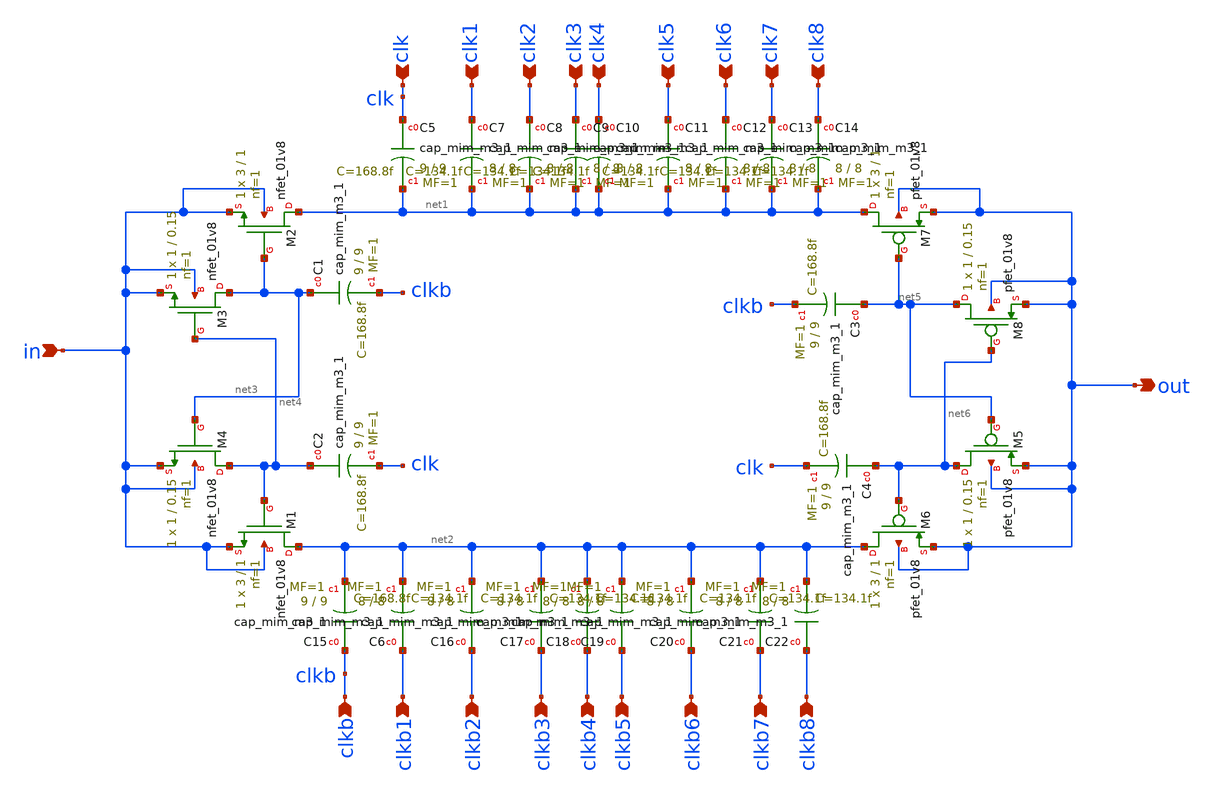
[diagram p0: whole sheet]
** sch_path: xschem/charge_pumps2/CP1.sch
**.subckt CP1 in clk clk1 clk2 clk3 clk4 clk5 clk6 clk7 clk8 clkb clkb1 clkb2 clkb3 clkb4 clkb5
*+ clkb6 clkb7 clkb8 out
*.ipin in
*.ipin clk
*.ipin clk1
*.ipin clk2
*.ipin clk3
*.ipin clk4
*.ipin clk5
*.ipin clk6
*.ipin clk7
*.ipin clk8
*.ipin clkb
*.ipin clkb1
*.ipin clkb2
*.ipin clkb3
*.ipin clkb4
*.ipin clkb5
*.ipin clkb6
*.ipin clkb7
*.ipin clkb8
*.opin out
XM2 net1 net3 in in sky130_fd_pr__nfet_01v8 L=1 W=3 nf=1 ad='int((nf+1)/2) * W/nf * 0.29' as='int((nf+2)/2) * W/nf * 0.29'
+ pd='2*int((nf+1)/2) * (W/nf + 0.29)' ps='2*int((nf+2)/2) * (W/nf + 0.29)' nrd='0.29 / W' nrs='0.29 / W'
+ sa=0 sb=0 sd=0 mult=1 m=1
XM1 net2 net4 in in sky130_fd_pr__nfet_01v8 L=1 W=3 nf=1 ad='int((nf+1)/2) * W/nf * 0.29' as='int((nf+2)/2) * W/nf * 0.29'
+ pd='2*int((nf+1)/2) * (W/nf + 0.29)' ps='2*int((nf+2)/2) * (W/nf + 0.29)' nrd='0.29 / W' nrs='0.29 / W'
+ sa=0 sb=0 sd=0 mult=1 m=1
XM3 net3 net4 in in sky130_fd_pr__nfet_01v8 L=0.15 W=1 nf=1 ad='int((nf+1)/2) * W/nf * 0.29' as='int((nf+2)/2) * W/nf * 0.29'
+ pd='2*int((nf+1)/2) * (W/nf + 0.29)' ps='2*int((nf+2)/2) * (W/nf + 0.29)' nrd='0.29 / W' nrs='0.29 / W'
+ sa=0 sb=0 sd=0 mult=1 m=1
XM4 net4 net3 in in sky130_fd_pr__nfet_01v8 L=0.15 W=1 nf=1 ad='int((nf+1)/2) * W/nf * 0.29' as='int((nf+2)/2) * W/nf * 0.29'
+ pd='2*int((nf+1)/2) * (W/nf + 0.29)' ps='2*int((nf+2)/2) * (W/nf + 0.29)' nrd='0.29 / W' nrs='0.29 / W'
+ sa=0 sb=0 sd=0 mult=1 m=1
XM5 net6 net5 out out sky130_fd_pr__pfet_01v8 L=0.15 W=1 nf=1 ad='int((nf+1)/2) * W/nf * 0.29' as='int((nf+2)/2) * W/nf * 0.29'
+ pd='2*int((nf+1)/2) * (W/nf + 0.29)' ps='2*int((nf+2)/2) * (W/nf + 0.29)' nrd='0.29 / W' nrs='0.29 / W'
+ sa=0 sb=0 sd=0 mult=1 m=1
XM6 net2 net6 out out sky130_fd_pr__pfet_01v8 L=1 W=3 nf=1 ad='int((nf+1)/2) * W/nf * 0.29' as='int((nf+2)/2) * W/nf * 0.29'
+ pd='2*int((nf+1)/2) * (W/nf + 0.29)' ps='2*int((nf+2)/2) * (W/nf + 0.29)' nrd='0.29 / W' nrs='0.29 / W'
+ sa=0 sb=0 sd=0 mult=1 m=1
XM7 net1 net5 out out sky130_fd_pr__pfet_01v8 L=1 W=3 nf=1 ad='int((nf+1)/2) * W/nf * 0.29' as='int((nf+2)/2) * W/nf * 0.29'
+ pd='2*int((nf+1)/2) * (W/nf + 0.29)' ps='2*int((nf+2)/2) * (W/nf + 0.29)' nrd='0.29 / W' nrs='0.29 / W'
+ sa=0 sb=0 sd=0 mult=1 m=1
XM8 net5 net6 out out sky130_fd_pr__pfet_01v8 L=0.15 W=1 nf=1 ad='int((nf+1)/2) * W/nf * 0.29' as='int((nf+2)/2) * W/nf * 0.29'
+ pd='2*int((nf+1)/2) * (W/nf + 0.29)' ps='2*int((nf+2)/2) * (W/nf + 0.29)' nrd='0.29 / W' nrs='0.29 / W'
+ sa=0 sb=0 sd=0 mult=1 m=1
XC1 net3 clkb sky130_fd_pr__cap_mim_m3_1 W=9 L=9 MF=1 m=1
XC2 net4 clk sky130_fd_pr__cap_mim_m3_1 W=9 L=9 MF=1 m=1
XC3 net5 clkb sky130_fd_pr__cap_mim_m3_1 W=9 L=9 MF=1 m=1
XC4 net6 clk sky130_fd_pr__cap_mim_m3_1 W=9 L=9 MF=1 m=1
XC5 clk net1 sky130_fd_pr__cap_mim_m3_1 W=9 L=9 MF=1 m=1
XC7 clk1 net1 sky130_fd_pr__cap_mim_m3_1 W=8 L=8 MF=1 m=1
XC8 clk2 net1 sky130_fd_pr__cap_mim_m3_1 W=8 L=8 MF=1 m=1
XC9 clk3 net1 sky130_fd_pr__cap_mim_m3_1 W=8 L=8 MF=1 m=1
XC10 clk4 net1 sky130_fd_pr__cap_mim_m3_1 W=8 L=8 MF=1 m=1
XC11 clk5 net1 sky130_fd_pr__cap_mim_m3_1 W=8 L=8 MF=1 m=1
XC12 clk6 net1 sky130_fd_pr__cap_mim_m3_1 W=8 L=8 MF=1 m=1
XC13 clk7 net1 sky130_fd_pr__cap_mim_m3_1 W=8 L=8 MF=1 m=1
XC14 clk8 net1 sky130_fd_pr__cap_mim_m3_1 W=8 L=8 MF=1 m=1
XC16 clkb2 net2 sky130_fd_pr__cap_mim_m3_1 W=8 L=8 MF=1 m=1
XC17 clkb3 net2 sky130_fd_pr__cap_mim_m3_1 W=8 L=8 MF=1 m=1
XC18 clkb4 net2 sky130_fd_pr__cap_mim_m3_1 W=8 L=8 MF=1 m=1
XC19 clkb5 net2 sky130_fd_pr__cap_mim_m3_1 W=8 L=8 MF=1 m=1
XC20 clkb6 net2 sky130_fd_pr__cap_mim_m3_1 W=8 L=8 MF=1 m=1
XC21 clkb7 net2 sky130_fd_pr__cap_mim_m3_1 W=8 L=8 MF=1 m=1
XC22 clkb8 net2 sky130_fd_pr__cap_mim_m3_1 W=8 L=8 MF=1 m=1
XC6 clkb1 net2 sky130_fd_pr__cap_mim_m3_1 W=8 L=8 MF=1 m=1
XC15 clkb net2 sky130_fd_pr__cap_mim_m3_1 W=9 L=9 MF=1 m=1
**.ends
.end
